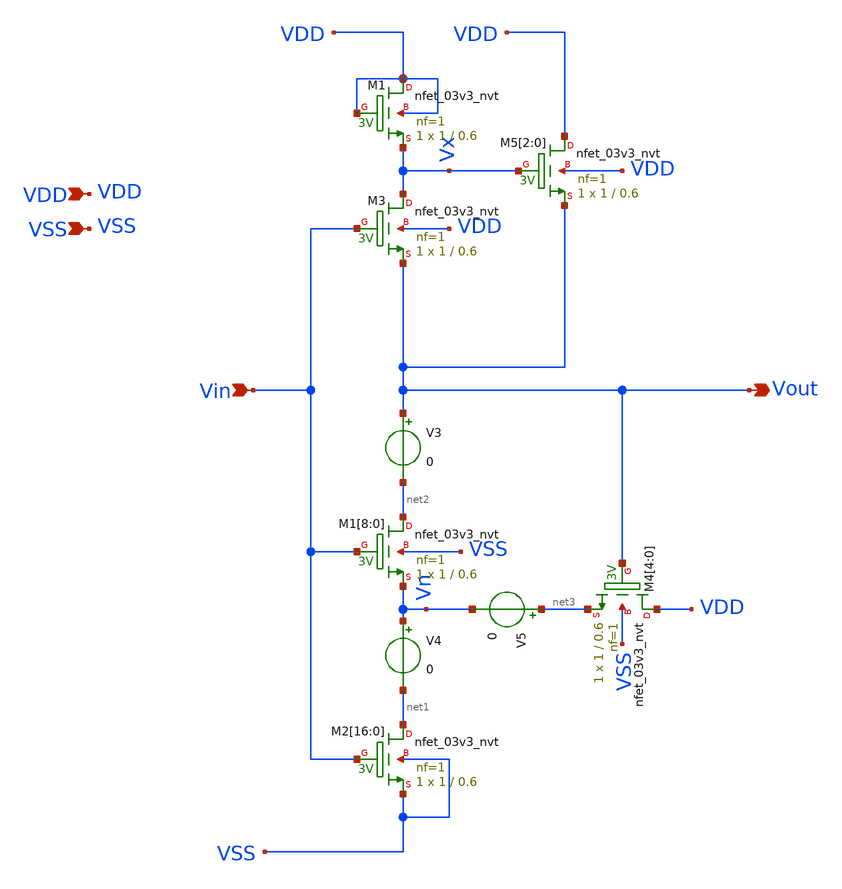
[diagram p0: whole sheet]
** sch_path: design/THESIS_EXP_RO_INVERTER_SKY130A/INV_NVT_no_pfet.sch
**.subckt INV_NVT_no_pfet VSS Vin Vout VDD
*.ipin VSS
*.ipin Vin
*.opin Vout
*.ipin VDD
V3 Vout net2 0
.save i(v3)
V4 Vn net1 0
.save i(v4)
V5 net3 Vn 0
.save i(v5)
XM1[8] net2 Vin Vn VSS sky130_fd_pr__nfet_03v3_nvt L=0.6 W=1 nf=1 ad='int((1 + 1)/2) * 1 / 1 * 0.29'
+ as='int((1 + 2)/2) * 1 / 1 * 0.29' pd='2*int((1 + 1)/2) * (1 / 1 + 0.29)' ps='2*int((1 + 2)/2) * (1 / 1 + 0.29)'
+ nrd='0.29 / 1 ' nrs='0.29 / 1 ' sa=0 sb=0 sd=0 mult=1 m=1
XM1[7] net2 Vin Vn VSS sky130_fd_pr__nfet_03v3_nvt L=0.6 W=1 nf=1 ad='int((1 + 1)/2) * 1 / 1 * 0.29'
+ as='int((1 + 2)/2) * 1 / 1 * 0.29' pd='2*int((1 + 1)/2) * (1 / 1 + 0.29)' ps='2*int((1 + 2)/2) * (1 / 1 + 0.29)'
+ nrd='0.29 / 1 ' nrs='0.29 / 1 ' sa=0 sb=0 sd=0 mult=1 m=1
XM1[6] net2 Vin Vn VSS sky130_fd_pr__nfet_03v3_nvt L=0.6 W=1 nf=1 ad='int((1 + 1)/2) * 1 / 1 * 0.29'
+ as='int((1 + 2)/2) * 1 / 1 * 0.29' pd='2*int((1 + 1)/2) * (1 / 1 + 0.29)' ps='2*int((1 + 2)/2) * (1 / 1 + 0.29)'
+ nrd='0.29 / 1 ' nrs='0.29 / 1 ' sa=0 sb=0 sd=0 mult=1 m=1
XM1[5] net2 Vin Vn VSS sky130_fd_pr__nfet_03v3_nvt L=0.6 W=1 nf=1 ad='int((1 + 1)/2) * 1 / 1 * 0.29'
+ as='int((1 + 2)/2) * 1 / 1 * 0.29' pd='2*int((1 + 1)/2) * (1 / 1 + 0.29)' ps='2*int((1 + 2)/2) * (1 / 1 + 0.29)'
+ nrd='0.29 / 1 ' nrs='0.29 / 1 ' sa=0 sb=0 sd=0 mult=1 m=1
XM1[4] net2 Vin Vn VSS sky130_fd_pr__nfet_03v3_nvt L=0.6 W=1 nf=1 ad='int((1 + 1)/2) * 1 / 1 * 0.29'
+ as='int((1 + 2)/2) * 1 / 1 * 0.29' pd='2*int((1 + 1)/2) * (1 / 1 + 0.29)' ps='2*int((1 + 2)/2) * (1 / 1 + 0.29)'
+ nrd='0.29 / 1 ' nrs='0.29 / 1 ' sa=0 sb=0 sd=0 mult=1 m=1
XM1[3] net2 Vin Vn VSS sky130_fd_pr__nfet_03v3_nvt L=0.6 W=1 nf=1 ad='int((1 + 1)/2) * 1 / 1 * 0.29'
+ as='int((1 + 2)/2) * 1 / 1 * 0.29' pd='2*int((1 + 1)/2) * (1 / 1 + 0.29)' ps='2*int((1 + 2)/2) * (1 / 1 + 0.29)'
+ nrd='0.29 / 1 ' nrs='0.29 / 1 ' sa=0 sb=0 sd=0 mult=1 m=1
XM1[2] net2 Vin Vn VSS sky130_fd_pr__nfet_03v3_nvt L=0.6 W=1 nf=1 ad='int((1 + 1)/2) * 1 / 1 * 0.29'
+ as='int((1 + 2)/2) * 1 / 1 * 0.29' pd='2*int((1 + 1)/2) * (1 / 1 + 0.29)' ps='2*int((1 + 2)/2) * (1 / 1 + 0.29)'
+ nrd='0.29 / 1 ' nrs='0.29 / 1 ' sa=0 sb=0 sd=0 mult=1 m=1
XM1[1] net2 Vin Vn VSS sky130_fd_pr__nfet_03v3_nvt L=0.6 W=1 nf=1 ad='int((1 + 1)/2) * 1 / 1 * 0.29'
+ as='int((1 + 2)/2) * 1 / 1 * 0.29' pd='2*int((1 + 1)/2) * (1 / 1 + 0.29)' ps='2*int((1 + 2)/2) * (1 / 1 + 0.29)'
+ nrd='0.29 / 1 ' nrs='0.29 / 1 ' sa=0 sb=0 sd=0 mult=1 m=1
XM1[0] net2 Vin Vn VSS sky130_fd_pr__nfet_03v3_nvt L=0.6 W=1 nf=1 ad='int((1 + 1)/2) * 1 / 1 * 0.29'
+ as='int((1 + 2)/2) * 1 / 1 * 0.29' pd='2*int((1 + 1)/2) * (1 / 1 + 0.29)' ps='2*int((1 + 2)/2) * (1 / 1 + 0.29)'
+ nrd='0.29 / 1 ' nrs='0.29 / 1 ' sa=0 sb=0 sd=0 mult=1 m=1
XM2[16] net1 Vin VSS VSS sky130_fd_pr__nfet_03v3_nvt L=0.6 W=1 nf=1 ad='int((1 + 1)/2) * 1 / 1 * 0.29'
+ as='int((1 + 2)/2) * 1 / 1 * 0.29' pd='2*int((1 + 1)/2) * (1 / 1 + 0.29)' ps='2*int((1 + 2)/2) * (1 / 1 + 0.29)'
+ nrd='0.29 / 1 ' nrs='0.29 / 1 ' sa=0 sb=0 sd=0 mult=1 m=1
XM2[15] net1 Vin VSS VSS sky130_fd_pr__nfet_03v3_nvt L=0.6 W=1 nf=1 ad='int((1 + 1)/2) * 1 / 1 * 0.29'
+ as='int((1 + 2)/2) * 1 / 1 * 0.29' pd='2*int((1 + 1)/2) * (1 / 1 + 0.29)' ps='2*int((1 + 2)/2) * (1 / 1 + 0.29)'
+ nrd='0.29 / 1 ' nrs='0.29 / 1 ' sa=0 sb=0 sd=0 mult=1 m=1
XM2[14] net1 Vin VSS VSS sky130_fd_pr__nfet_03v3_nvt L=0.6 W=1 nf=1 ad='int((1 + 1)/2) * 1 / 1 * 0.29'
+ as='int((1 + 2)/2) * 1 / 1 * 0.29' pd='2*int((1 + 1)/2) * (1 / 1 + 0.29)' ps='2*int((1 + 2)/2) * (1 / 1 + 0.29)'
+ nrd='0.29 / 1 ' nrs='0.29 / 1 ' sa=0 sb=0 sd=0 mult=1 m=1
XM2[13] net1 Vin VSS VSS sky130_fd_pr__nfet_03v3_nvt L=0.6 W=1 nf=1 ad='int((1 + 1)/2) * 1 / 1 * 0.29'
+ as='int((1 + 2)/2) * 1 / 1 * 0.29' pd='2*int((1 + 1)/2) * (1 / 1 + 0.29)' ps='2*int((1 + 2)/2) * (1 / 1 + 0.29)'
+ nrd='0.29 / 1 ' nrs='0.29 / 1 ' sa=0 sb=0 sd=0 mult=1 m=1
XM2[12] net1 Vin VSS VSS sky130_fd_pr__nfet_03v3_nvt L=0.6 W=1 nf=1 ad='int((1 + 1)/2) * 1 / 1 * 0.29'
+ as='int((1 + 2)/2) * 1 / 1 * 0.29' pd='2*int((1 + 1)/2) * (1 / 1 + 0.29)' ps='2*int((1 + 2)/2) * (1 / 1 + 0.29)'
+ nrd='0.29 / 1 ' nrs='0.29 / 1 ' sa=0 sb=0 sd=0 mult=1 m=1
XM2[11] net1 Vin VSS VSS sky130_fd_pr__nfet_03v3_nvt L=0.6 W=1 nf=1 ad='int((1 + 1)/2) * 1 / 1 * 0.29'
+ as='int((1 + 2)/2) * 1 / 1 * 0.29' pd='2*int((1 + 1)/2) * (1 / 1 + 0.29)' ps='2*int((1 + 2)/2) * (1 / 1 + 0.29)'
+ nrd='0.29 / 1 ' nrs='0.29 / 1 ' sa=0 sb=0 sd=0 mult=1 m=1
XM2[10] net1 Vin VSS VSS sky130_fd_pr__nfet_03v3_nvt L=0.6 W=1 nf=1 ad='int((1 + 1)/2) * 1 / 1 * 0.29'
+ as='int((1 + 2)/2) * 1 / 1 * 0.29' pd='2*int((1 + 1)/2) * (1 / 1 + 0.29)' ps='2*int((1 + 2)/2) * (1 / 1 + 0.29)'
+ nrd='0.29 / 1 ' nrs='0.29 / 1 ' sa=0 sb=0 sd=0 mult=1 m=1
XM2[9] net1 Vin VSS VSS sky130_fd_pr__nfet_03v3_nvt L=0.6 W=1 nf=1 ad='int((1 + 1)/2) * 1 / 1 * 0.29'
+ as='int((1 + 2)/2) * 1 / 1 * 0.29' pd='2*int((1 + 1)/2) * (1 / 1 + 0.29)' ps='2*int((1 + 2)/2) * (1 / 1 + 0.29)'
+ nrd='0.29 / 1 ' nrs='0.29 / 1 ' sa=0 sb=0 sd=0 mult=1 m=1
XM2[8] net1 Vin VSS VSS sky130_fd_pr__nfet_03v3_nvt L=0.6 W=1 nf=1 ad='int((1 + 1)/2) * 1 / 1 * 0.29'
+ as='int((1 + 2)/2) * 1 / 1 * 0.29' pd='2*int((1 + 1)/2) * (1 / 1 + 0.29)' ps='2*int((1 + 2)/2) * (1 / 1 + 0.29)'
+ nrd='0.29 / 1 ' nrs='0.29 / 1 ' sa=0 sb=0 sd=0 mult=1 m=1
XM2[7] net1 Vin VSS VSS sky130_fd_pr__nfet_03v3_nvt L=0.6 W=1 nf=1 ad='int((1 + 1)/2) * 1 / 1 * 0.29'
+ as='int((1 + 2)/2) * 1 / 1 * 0.29' pd='2*int((1 + 1)/2) * (1 / 1 + 0.29)' ps='2*int((1 + 2)/2) * (1 / 1 + 0.29)'
+ nrd='0.29 / 1 ' nrs='0.29 / 1 ' sa=0 sb=0 sd=0 mult=1 m=1
XM2[6] net1 Vin VSS VSS sky130_fd_pr__nfet_03v3_nvt L=0.6 W=1 nf=1 ad='int((1 + 1)/2) * 1 / 1 * 0.29'
+ as='int((1 + 2)/2) * 1 / 1 * 0.29' pd='2*int((1 + 1)/2) * (1 / 1 + 0.29)' ps='2*int((1 + 2)/2) * (1 / 1 + 0.29)'
+ nrd='0.29 / 1 ' nrs='0.29 / 1 ' sa=0 sb=0 sd=0 mult=1 m=1
XM2[5] net1 Vin VSS VSS sky130_fd_pr__nfet_03v3_nvt L=0.6 W=1 nf=1 ad='int((1 + 1)/2) * 1 / 1 * 0.29'
+ as='int((1 + 2)/2) * 1 / 1 * 0.29' pd='2*int((1 + 1)/2) * (1 / 1 + 0.29)' ps='2*int((1 + 2)/2) * (1 / 1 + 0.29)'
+ nrd='0.29 / 1 ' nrs='0.29 / 1 ' sa=0 sb=0 sd=0 mult=1 m=1
XM2[4] net1 Vin VSS VSS sky130_fd_pr__nfet_03v3_nvt L=0.6 W=1 nf=1 ad='int((1 + 1)/2) * 1 / 1 * 0.29'
+ as='int((1 + 2)/2) * 1 / 1 * 0.29' pd='2*int((1 + 1)/2) * (1 / 1 + 0.29)' ps='2*int((1 + 2)/2) * (1 / 1 + 0.29)'
+ nrd='0.29 / 1 ' nrs='0.29 / 1 ' sa=0 sb=0 sd=0 mult=1 m=1
XM2[3] net1 Vin VSS VSS sky130_fd_pr__nfet_03v3_nvt L=0.6 W=1 nf=1 ad='int((1 + 1)/2) * 1 / 1 * 0.29'
+ as='int((1 + 2)/2) * 1 / 1 * 0.29' pd='2*int((1 + 1)/2) * (1 / 1 + 0.29)' ps='2*int((1 + 2)/2) * (1 / 1 + 0.29)'
+ nrd='0.29 / 1 ' nrs='0.29 / 1 ' sa=0 sb=0 sd=0 mult=1 m=1
XM2[2] net1 Vin VSS VSS sky130_fd_pr__nfet_03v3_nvt L=0.6 W=1 nf=1 ad='int((1 + 1)/2) * 1 / 1 * 0.29'
+ as='int((1 + 2)/2) * 1 / 1 * 0.29' pd='2*int((1 + 1)/2) * (1 / 1 + 0.29)' ps='2*int((1 + 2)/2) * (1 / 1 + 0.29)'
+ nrd='0.29 / 1 ' nrs='0.29 / 1 ' sa=0 sb=0 sd=0 mult=1 m=1
XM2[1] net1 Vin VSS VSS sky130_fd_pr__nfet_03v3_nvt L=0.6 W=1 nf=1 ad='int((1 + 1)/2) * 1 / 1 * 0.29'
+ as='int((1 + 2)/2) * 1 / 1 * 0.29' pd='2*int((1 + 1)/2) * (1 / 1 + 0.29)' ps='2*int((1 + 2)/2) * (1 / 1 + 0.29)'
+ nrd='0.29 / 1 ' nrs='0.29 / 1 ' sa=0 sb=0 sd=0 mult=1 m=1
XM2[0] net1 Vin VSS VSS sky130_fd_pr__nfet_03v3_nvt L=0.6 W=1 nf=1 ad='int((1 + 1)/2) * 1 / 1 * 0.29'
+ as='int((1 + 2)/2) * 1 / 1 * 0.29' pd='2*int((1 + 1)/2) * (1 / 1 + 0.29)' ps='2*int((1 + 2)/2) * (1 / 1 + 0.29)'
+ nrd='0.29 / 1 ' nrs='0.29 / 1 ' sa=0 sb=0 sd=0 mult=1 m=1
XM4[4] VDD Vout net3 VSS sky130_fd_pr__nfet_03v3_nvt L=0.6 W=1 nf=1 ad='int((1 + 1)/2) * 1 / 1 * 0.29'
+ as='int((1 + 2)/2) * 1 / 1 * 0.29' pd='2*int((1 + 1)/2) * (1 / 1 + 0.29)' ps='2*int((1 + 2)/2) * (1 / 1 + 0.29)'
+ nrd='0.29 / 1 ' nrs='0.29 / 1 ' sa=0 sb=0 sd=0 mult=1 m=1
XM4[3] VDD Vout net3 VSS sky130_fd_pr__nfet_03v3_nvt L=0.6 W=1 nf=1 ad='int((1 + 1)/2) * 1 / 1 * 0.29'
+ as='int((1 + 2)/2) * 1 / 1 * 0.29' pd='2*int((1 + 1)/2) * (1 / 1 + 0.29)' ps='2*int((1 + 2)/2) * (1 / 1 + 0.29)'
+ nrd='0.29 / 1 ' nrs='0.29 / 1 ' sa=0 sb=0 sd=0 mult=1 m=1
XM4[2] VDD Vout net3 VSS sky130_fd_pr__nfet_03v3_nvt L=0.6 W=1 nf=1 ad='int((1 + 1)/2) * 1 / 1 * 0.29'
+ as='int((1 + 2)/2) * 1 / 1 * 0.29' pd='2*int((1 + 1)/2) * (1 / 1 + 0.29)' ps='2*int((1 + 2)/2) * (1 / 1 + 0.29)'
+ nrd='0.29 / 1 ' nrs='0.29 / 1 ' sa=0 sb=0 sd=0 mult=1 m=1
XM4[1] VDD Vout net3 VSS sky130_fd_pr__nfet_03v3_nvt L=0.6 W=1 nf=1 ad='int((1 + 1)/2) * 1 / 1 * 0.29'
+ as='int((1 + 2)/2) * 1 / 1 * 0.29' pd='2*int((1 + 1)/2) * (1 / 1 + 0.29)' ps='2*int((1 + 2)/2) * (1 / 1 + 0.29)'
+ nrd='0.29 / 1 ' nrs='0.29 / 1 ' sa=0 sb=0 sd=0 mult=1 m=1
XM4[0] VDD Vout net3 VSS sky130_fd_pr__nfet_03v3_nvt L=0.6 W=1 nf=1 ad='int((1 + 1)/2) * 1 / 1 * 0.29'
+ as='int((1 + 2)/2) * 1 / 1 * 0.29' pd='2*int((1 + 1)/2) * (1 / 1 + 0.29)' ps='2*int((1 + 2)/2) * (1 / 1 + 0.29)'
+ nrd='0.29 / 1 ' nrs='0.29 / 1 ' sa=0 sb=0 sd=0 mult=1 m=1
XM3 Vx Vin Vout VDD sky130_fd_pr__nfet_03v3_nvt L=0.6 W=1 nf=1 ad='int((1 + 1)/2) * 1 / 1 * 0.29' as='int((1 + 2)/2) * 1 / 1 * 0.29'
+ pd='2*int((1 + 1)/2) * (1 / 1 + 0.29)' ps='2*int((1 + 2)/2) * (1 / 1 + 0.29)' nrd='0.29 / 1 ' nrs='0.29 / 1 '
+ sa=0 sb=0 sd=0 mult=1 m=1
XM1 VDD VDD Vx VDD sky130_fd_pr__nfet_03v3_nvt L=0.6 W=1 nf=1 ad='int((1 + 1)/2) * 1 / 1 * 0.29' as='int((1 + 2)/2) * 1 / 1 * 0.29'
+ pd='2*int((1 + 1)/2) * (1 / 1 + 0.29)' ps='2*int((1 + 2)/2) * (1 / 1 + 0.29)' nrd='0.29 / 1 ' nrs='0.29 / 1 '
+ sa=0 sb=0 sd=0 mult=1 m=1
XM5[2] VDD Vx Vout VDD sky130_fd_pr__nfet_03v3_nvt L=0.6 W=1 nf=1 ad='int((1 + 1)/2) * 1 / 1 * 0.29'
+ as='int((1 + 2)/2) * 1 / 1 * 0.29' pd='2*int((1 + 1)/2) * (1 / 1 + 0.29)' ps='2*int((1 + 2)/2) * (1 / 1 + 0.29)'
+ nrd='0.29 / 1 ' nrs='0.29 / 1 ' sa=0 sb=0 sd=0 mult=1 m=1
XM5[1] VDD Vx Vout VDD sky130_fd_pr__nfet_03v3_nvt L=0.6 W=1 nf=1 ad='int((1 + 1)/2) * 1 / 1 * 0.29'
+ as='int((1 + 2)/2) * 1 / 1 * 0.29' pd='2*int((1 + 1)/2) * (1 / 1 + 0.29)' ps='2*int((1 + 2)/2) * (1 / 1 + 0.29)'
+ nrd='0.29 / 1 ' nrs='0.29 / 1 ' sa=0 sb=0 sd=0 mult=1 m=1
XM5[0] VDD Vx Vout VDD sky130_fd_pr__nfet_03v3_nvt L=0.6 W=1 nf=1 ad='int((1 + 1)/2) * 1 / 1 * 0.29'
+ as='int((1 + 2)/2) * 1 / 1 * 0.29' pd='2*int((1 + 1)/2) * (1 / 1 + 0.29)' ps='2*int((1 + 2)/2) * (1 / 1 + 0.29)'
+ nrd='0.29 / 1 ' nrs='0.29 / 1 ' sa=0 sb=0 sd=0 mult=1 m=1
**.ends
.end
